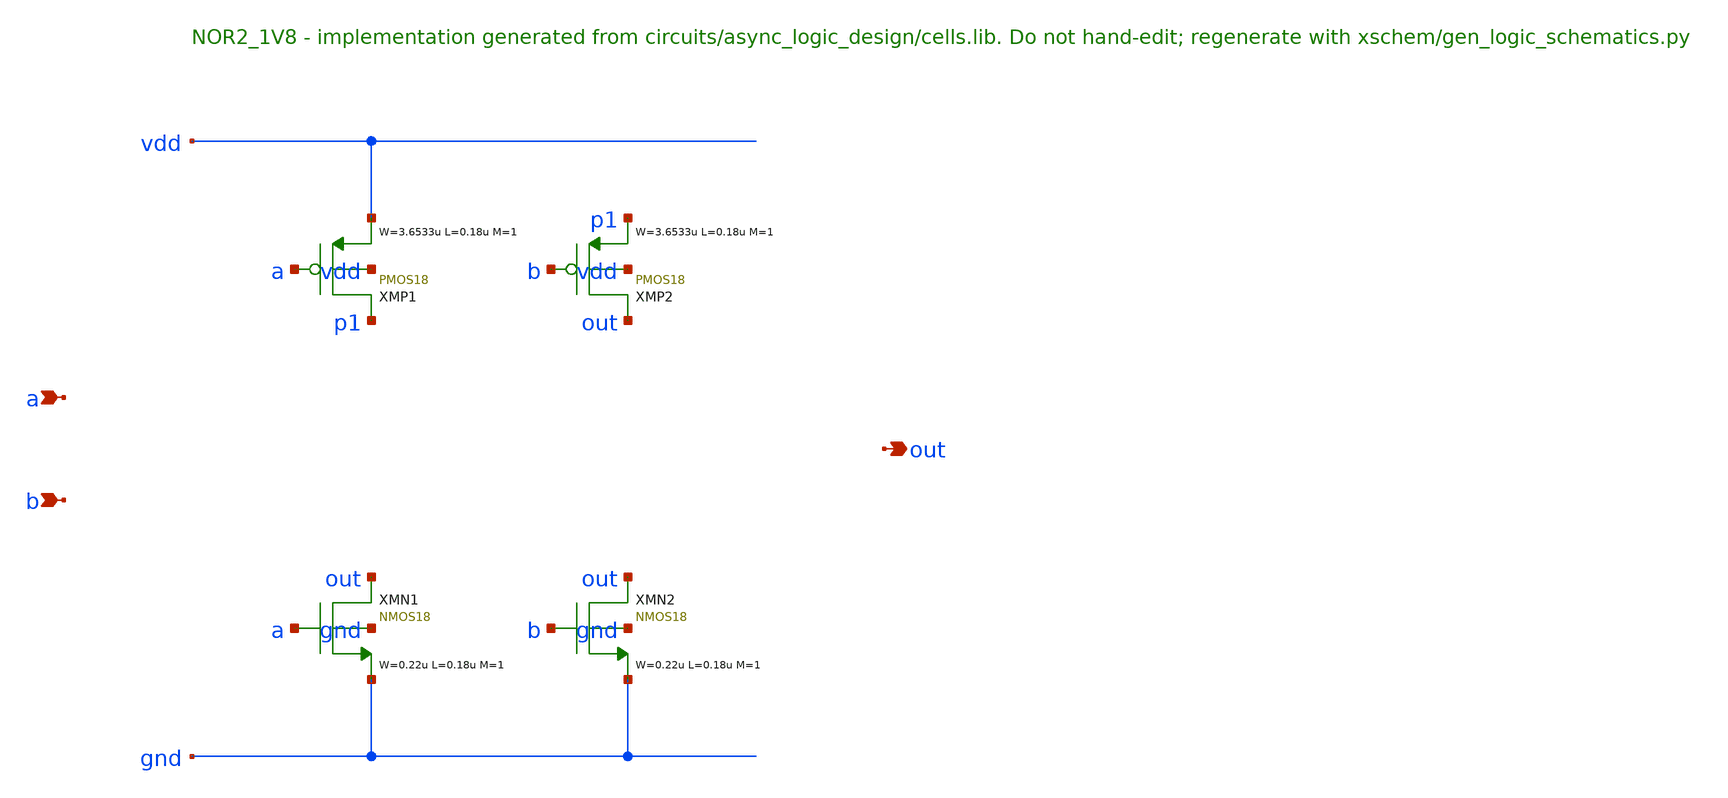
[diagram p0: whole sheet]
** sch_path: xschem/logic/NOR2_1V8.sch
**.subckt NOR2_1V8 a b out
*.ipin a
*.ipin b
*.opin out
XMP1 p1 a vdd vdd PMOS18 W=3.6533u L=0.18u M=1 MM_SIGMA=0
XMP2 out b p1 vdd PMOS18 W=3.6533u L=0.18u M=1 MM_SIGMA=0
XMN1 out a gnd gnd NMOS18 W=0.22u L=0.18u M=1 MM_SIGMA=0
XMN2 out b gnd gnd NMOS18 W=0.22u L=0.18u M=1 MM_SIGMA=0
**.ends
.end
